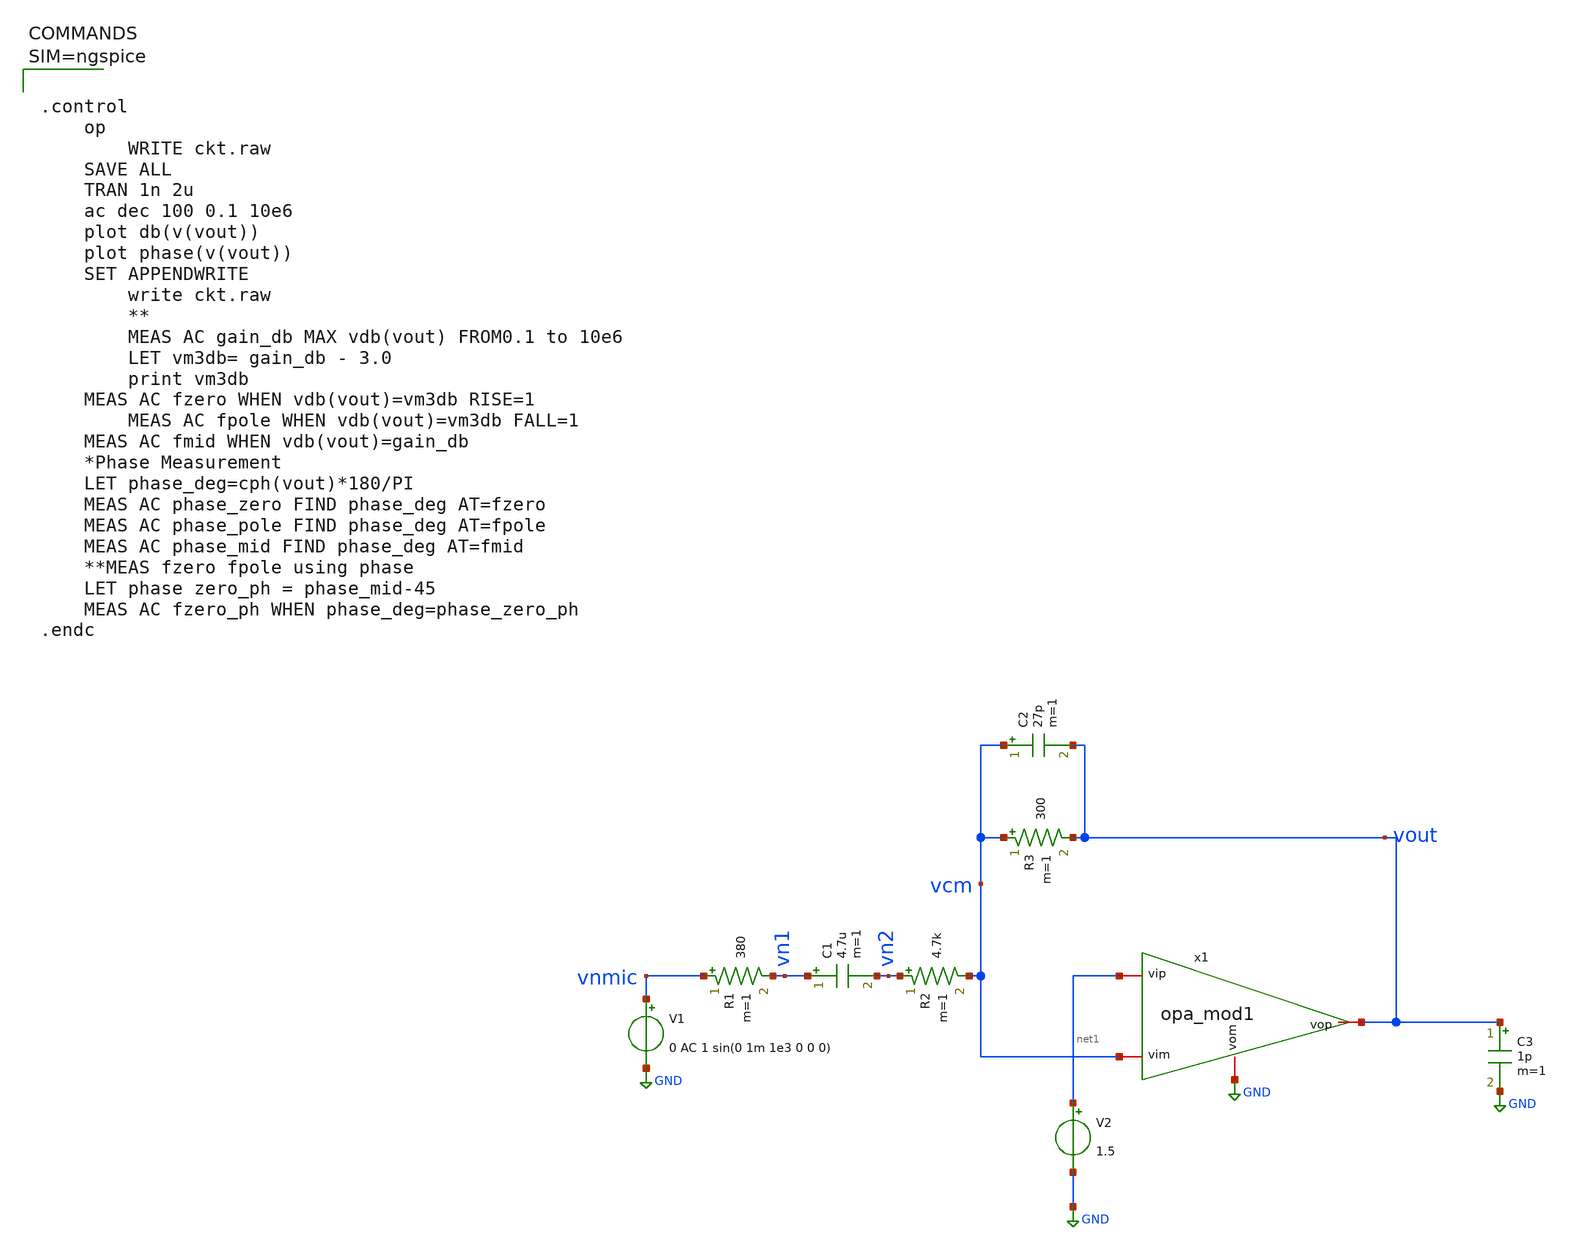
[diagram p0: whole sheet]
** sch_path: xschem/micTestOpa_mod1.sch
**.subckt micTestOpa_mod1
V1 vnmic GND 0 AC 1 sin(0 1m 1e3 0 0 0)
C1 vn1 vn2 4.7u m=1
R1 vnmic vn1 380 m=1
R2 vn2 vcm 4.7k m=1
R3 vcm vout 300 m=1
C2 vcm vout 27p m=1
C3 vout GND 1p m=1
V2 net1 GND 1.5
x1 vout net1 vcm GND opa_mod1
**** begin user architecture code



.control
	op
        WRITE ckt.raw
	SAVE ALL
	TRAN 1n 2u
	ac dec 100 0.1 10e6
	plot db(v(vout))
	plot phase(v(vout))
	SET APPENDWRITE
        write ckt.raw
        **
        MEAS AC gain_db MAX vdb(vout) FROM0.1 to 10e6
        LET vm3db= gain_db - 3.0
        print vm3db
	MEAS AC fzero WHEN vdb(vout)=vm3db RISE=1
        MEAS AC fpole WHEN vdb(vout)=vm3db FALL=1
	MEAS AC fmid WHEN vdb(vout)=gain_db
	*Phase Measurement
	LET phase_deg=cph(vout)*180/PI
	MEAS AC phase_zero FIND phase_deg AT=fzero
	MEAS AC phase_pole FIND phase_deg AT=fpole
	MEAS AC phase_mid FIND phase_deg AT=fmid
	**MEAS fzero fpole using phase
	LET phase zero_ph = phase_mid-45
	MEAS AC fzero_ph WHEN phase_deg=phase_zero_ph
.endc



**** end user architecture code
**.ends

* expanding   symbol:  opa_mod1.sym # of pins=4
** sym_path: xschem/opa_mod1.sym
** sch_path: xschem/opa_mod1.sch
.subckt opa_mod1 vop vip vim vom
*.iopin vop
*.iopin vom
*.iopin vim
*.iopin vip
E1 vop vom vip vim 1000
.ends

.GLOBAL GND
.end
